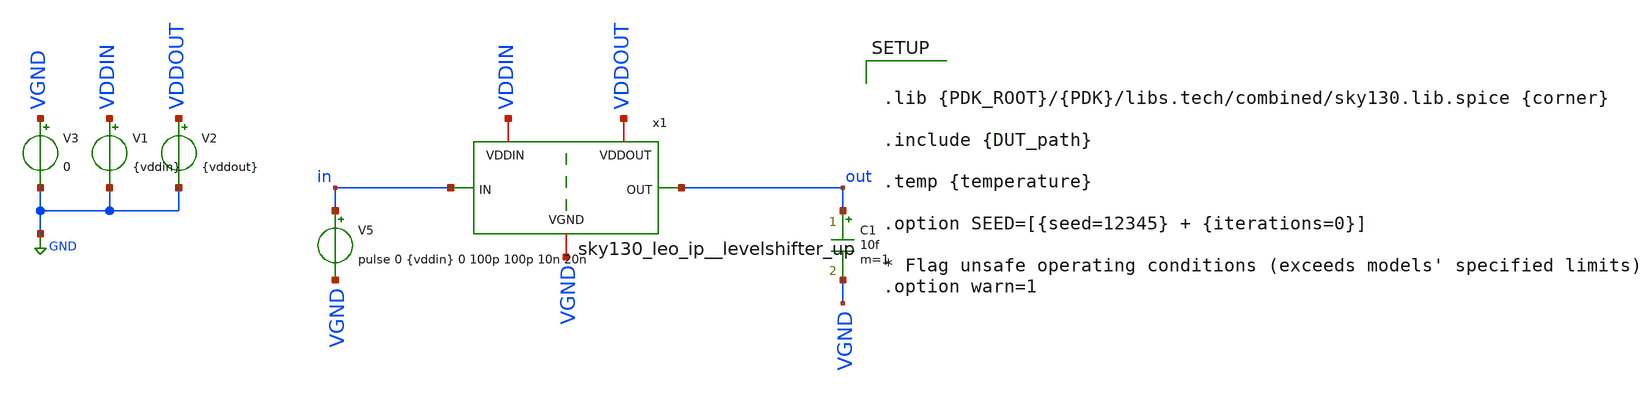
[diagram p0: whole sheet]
** sch_path: cace/templates/rise_fall_up.sch
**.subckt rise_fall_up
x1 VDDOUT VDDIN out in VGND sky130_leo_ip__levelshifter_up
V1 VDDIN GND {vddin}
V2 VDDOUT GND {vddout}
V3 VGND GND 0
C1 out VGND 10f m=1
V5 in VGND pulse 0 {vddin} 0 100p 100p 10n 20n
**** begin user architecture code




.control
    * operating point
    *op
    *write tb.raw
    *set appendwrite

    * transient simulation
    options method=gear
    tran 1p 40n
    *save all
    *write tb.raw

    * measure parameters

    * get the peak-to-peak voltage
    meas TRAN range PP v(out)
    let ten=0.1*range
    let ninety=0.9*range

    print range ten ninety

    # rise and fall time
    meas TRAN rise_time TRIG v(out) VAL=ten    TD=0ns  RISE=1   TARG v(out) VAL=ninety TD=0ns
+  RISE=1
    meas TRAN fall_time TRIG v(out) VAL=ninety TD=5ns  FALL=1   TARG v(out) VAL=TEN    TD=5ns
+  FALL=1

    print rise_time fall_time

    echo $&rise_time $&fall_time > {simpath}/{filename}_{N}.data

.endc





.lib {PDK_ROOT}/{PDK}/libs.tech/combined/sky130.lib.spice {corner}

.include {DUT_path}

.temp {temperature}

.option SEED=[{seed=12345} + {iterations=0}]

* Flag unsafe operating conditions (exceeds models' specified limits)
.option warn=1


**** end user architecture code
**.ends

* expanding   symbol:  sky130_leo_ip__levelshifter_up.sym # of pins=5
** sym_path: xschem/sky130_leo_ip__levelshifter_up.sym
** sch_path: xschem/sky130_leo_ip__levelshifter_up.sch
.subckt sky130_leo_ip__levelshifter_up VDDOUT VDDIN OUT IN VGND
*.ipin IN
*.iopin VGND
*.iopin VDDIN
*.ipin OUT
*.iopin VDDOUT
XM1 ctrl_n IN VGND VGND sky130_fd_pr__nfet_01v8 L=0.15 W=0.42 nf=1 ad='int((nf+1)/2) * W/nf * 0.29' as='int((nf+2)/2)
+ * W/nf * 0.29' pd='2*int((nf+1)/2) * (W/nf + 0.29)' ps='2*int((nf+2)/2) * (W/nf + 0.29)' nrd='0.29 /
+ W' nrs='0.29 / W' sa=0 sb=0 sd=0 mult=1 m=1
XM2 ctrl_n IN VDDIN VDDIN sky130_fd_pr__pfet_01v8 L=0.15 W=1 nf=1 ad='int((nf+1)/2) * W/nf * 0.29' as='int((nf+2)/2)
+ * W/nf * 0.29' pd='2*int((nf+1)/2) * (W/nf + 0.29)' ps='2*int((nf+2)/2) * (W/nf + 0.29)' nrd='0.29 /
+ W' nrs='0.29 / W' sa=0 sb=0 sd=0 mult=1 m=1
XM3 ctrl ctrl_n VGND VGND sky130_fd_pr__nfet_01v8 L=0.15 W=0.42 nf=1 ad='int((nf+1)/2) * W/nf * 0.29' as='int((nf+2)/2)
+ * W/nf * 0.29' pd='2*int((nf+1)/2) * (W/nf + 0.29)' ps='2*int((nf+2)/2) * (W/nf + 0.29)' nrd='0.29 /
+ W' nrs='0.29 / W' sa=0 sb=0 sd=0 mult=1 m=1
XM4 ctrl ctrl_n VDDIN VDDIN sky130_fd_pr__pfet_01v8 L=0.15 W=1 nf=1 ad='int((nf+1)/2) * W/nf * 0.29' as='int((nf+2)/2)
+ * W/nf * 0.29' pd='2*int((nf+1)/2) * (W/nf + 0.29)' ps='2*int((nf+2)/2) * (W/nf + 0.29)' nrd='0.29 /
+ W' nrs='0.29 / W' sa=0 sb=0 sd=0 mult=1 m=1
XM5 OUT p1 VDDOUT VDDOUT sky130_fd_pr__pfet_g5v0d10v5 L=0.5 W=0.42 nf=1 ad='int((nf+1)/2) * W/nf * 0.29' as='int((nf+2)/2)
+ * W/nf * 0.29' pd='2*int((nf+1)/2) * (W/nf + 0.29)' ps='2*int((nf+2)/2) * (W/nf + 0.29)' nrd='0.29 /
+ W' nrs='0.29 / W' sa=0 sb=0 sd=0 mult=1 m=1
XM6 p1 ctrl VGND VGND sky130_fd_pr__nfet_g5v0d10v5 L=0.5 W=1 nf=1 ad='int((nf+1)/2) * W/nf * 0.29' as='int((nf+2)/2)
+ * W/nf * 0.29' pd='2*int((nf+1)/2) * (W/nf + 0.29)' ps='2*int((nf+2)/2) * (W/nf + 0.29)' nrd='0.29 /
+ W' nrs='0.29 / W' sa=0 sb=0 sd=0 mult=1 m=1
XM7 p1 OUT VDDOUT VDDOUT sky130_fd_pr__pfet_g5v0d10v5 L=0.5 W=0.42 nf=1 ad='int((nf+1)/2) * W/nf * 0.29' as='int((nf+2)/2)
+ * W/nf * 0.29' pd='2*int((nf+1)/2) * (W/nf + 0.29)' ps='2*int((nf+2)/2) * (W/nf + 0.29)' nrd='0.29 /
+ W' nrs='0.29 / W' sa=0 sb=0 sd=0 mult=1 m=1
XM8 OUT ctrl_n VGND VGND sky130_fd_pr__nfet_g5v0d10v5 L=0.5 W=1 nf=1 ad='int((nf+1)/2) * W/nf * 0.29' as='int((nf+2)/2)
+ * W/nf * 0.29' pd='2*int((nf+1)/2) * (W/nf + 0.29)' ps='2*int((nf+2)/2) * (W/nf + 0.29)' nrd='0.29 /
+ W' nrs='0.29 / W' sa=0 sb=0 sd=0 mult=1 m=1
.ends

.GLOBAL GND
.end
